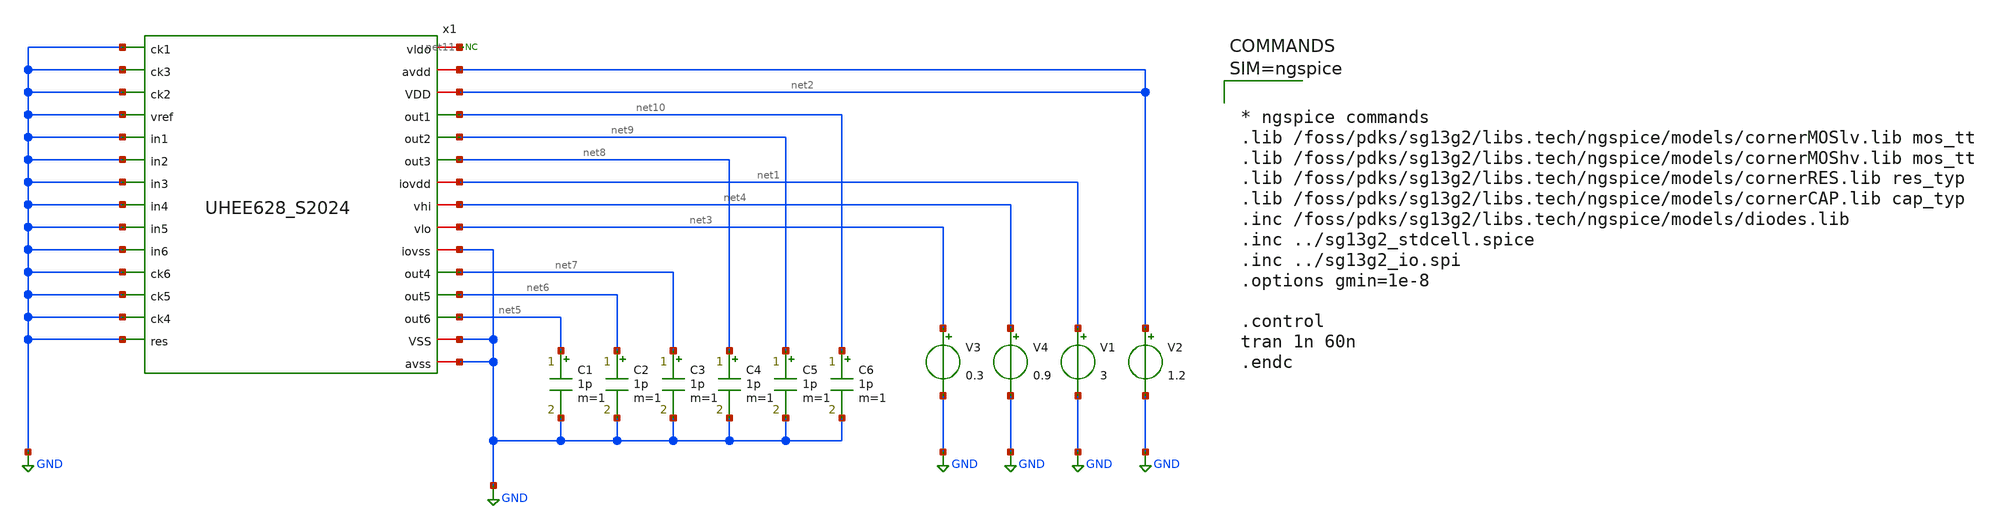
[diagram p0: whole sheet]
** sch_path: 5_Design/3_Real_circuits/tb_UHEE628_S2024.sch
**.subckt tb_UHEE628_S2024
x1 net11 GND GND net2 GND net2 GND net10 GND GND net9 net8 GND net1 net4 net3 GND net7 GND net6 GND
+ net5 GND GND GND GND GND GND GND UHEE628_S2024
V1 net1 GND 3
V2 net2 GND 1.2
* noconn #net11
V3 net3 GND 0.3
V4 net4 GND 0.9
C1 net5 GND 1p m=1
C2 net6 GND 1p m=1
C3 net7 GND 1p m=1
C4 net8 GND 1p m=1
C5 net9 GND 1p m=1
C6 net10 GND 1p m=1
**** begin user architecture code



* ngspice commands
.lib /foss/pdks/sg13g2/libs.tech/ngspice/models/cornerMOSlv.lib mos_tt
.lib /foss/pdks/sg13g2/libs.tech/ngspice/models/cornerMOShv.lib mos_tt
.lib /foss/pdks/sg13g2/libs.tech/ngspice/models/cornerRES.lib res_typ
.lib /foss/pdks/sg13g2/libs.tech/ngspice/models/cornerCAP.lib cap_typ
.inc /foss/pdks/sg13g2/libs.tech/ngspice/models/diodes.lib
.inc ../sg13g2_stdcell.spice
.inc ../sg13g2_io.spi
.options gmin=1e-8

.control
tran 1n 60n
.endc


**** end user architecture code
**.ends
.GLOBAL GND
.end
